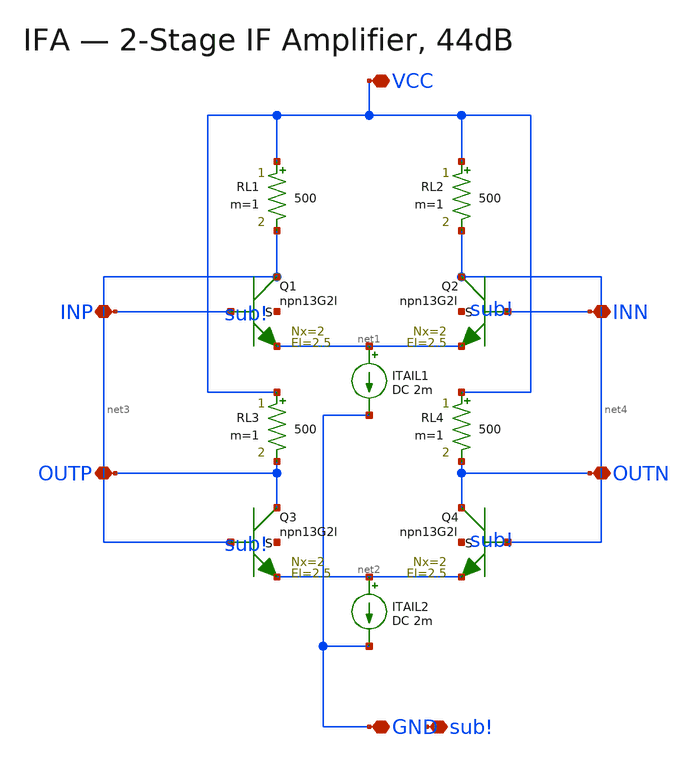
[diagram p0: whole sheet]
** sch_path: xschem/blocks/IFA_77G.sch
**.subckt IFA_77G INP INN OUTP OUTN VCC GND sub!
*.iopin INP
*.iopin INN
*.iopin OUTP
*.iopin OUTN
*.iopin VCC
*.iopin GND
*.iopin sub!
XQ1 net3 INP net1 sub! npn13G2l Nx=2 El=2.5 mm_ok=1
XQ2 net4 INN net1 sub! npn13G2l Nx=2 El=2.5 mm_ok=1
XQ3 OUTP net3 net2 sub! npn13G2l Nx=2 El=2.5 mm_ok=1
XQ4 OUTN net4 net2 sub! npn13G2l Nx=2 El=2.5 mm_ok=1
RL1 VCC net3 500 m=1
RL2 VCC net4 500 m=1
RL3 VCC OUTP 500 m=1
RL4 VCC OUTN 500 m=1
ITAIL1 net1 GND DC 2m
ITAIL2 net2 GND DC 2m
**.ends
.end
